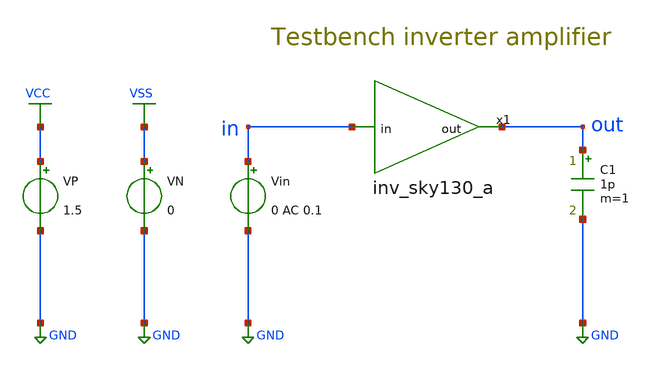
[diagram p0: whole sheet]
** sch_path: Amplifier_Inv/xschem/tb_inv_sky130_a.sch
* StefanSchippers/xschem_sky130/sky130_tests/not.sch:
* Copyright 2021 Stefan Frederik Schippers
* Licensed under the Apache License, Version 2.0 (the "License");
**.subckt tb_inv_sky130_a
x1 out in inv_sky130_a
Vin in GND 0 AC 0.1
VN VSS GND 0
VP VCC GND 1.5
C1 out GND 1p m=1
**** begin user architecture code

** opencircuitdesign pdks install
.lib $::SKYWATER_MODELS/sky130.lib.spice tt




.control
  tran 1ns 100us
  save all
  write tb_inv_sky130_a_tran.raw
  ac dec 10 0.1 100k
  save all
  let gain = db(v(out)/v(in))
  let phase = phase(v(out)/v(in))
  print gain phase
  write tb_inv_sky130_a_AC.raw gain phase
.endc


**** end user architecture code
**.ends

* expanding   symbol:  inv_sky130_a.sym # of pins=2
** sym_path: Amplifier_Inv/xschem/inv_sky130_a.sym
** sch_path: Amplifier_Inv/xschem/inv_sky130_a.sch
.subckt inv_sky130_a out in
*.ipin in
*.opin out
x1 out in VCC VSS not W_N=1 L_N=0.15 W_P=2 L_P=0.15 m=1
R1 out in sky130_fd_pr__res_generic_m1 W=1 L=1 m=1
R2 net1 out sky130_fd_pr__res_generic_m1 W=1 L=1 m=1
XC1 net1 GND sky130_fd_pr__cap_mim_m3_1 W=1 L=1 MF=1 m=1
.ends


* expanding   symbol:  sky130_tests/not.sym # of pins=2
** sym_path: sky130_tests/not.sym
** sch_path: sky130_tests/not.sch
.subckt not y a VCCPIN VSSPIN     W_N=1 L_N=0.15 W_P=2 L_P=0.15
*.opin y
*.ipin a
XM1 DN a VSSPIN VSSPIN sky130_fd_pr__nfet_01v8 L=L_N W=W_N nf=1 ad='int((1 + 1)/2) * W_N / 1 * 0.29'
+ as='int((1 + 2)/2) * W_N / 1 * 0.29' pd='2*int((1 + 1)/2) * (W_N / 1 + 0.29)' ps='2*int((1 + 2)/2) * (W_N / 1 + 0.29)'
+ nrd='0.29 / W_N ' nrs='0.29 / W_N ' sa=0 sb=0 sd=0 mult=1 m=1
XM2 DP a VCCPIN VCCPIN sky130_fd_pr__pfet_01v8 L=L_P W=W_P nf=1 ad='int((nf+1)/2) * W/nf * 0.29' as='int((nf+2)/2) * W/nf * 0.29'
+ pd='2*int((nf+1)/2) * (W/nf + 0.29)' ps='2*int((nf+2)/2) * (W/nf + 0.29)' nrd='0.29 / W' nrs='0.29 / W'
+ sa=0 sb=0 sd=0 mult=1 m=1
Vmeas DP y 0
.save i(vmeas)
Vmeas1 y DN 0
.save i(vmeas1)
.save v(dp)
.save v(dn)
.ends

.GLOBAL GND
.GLOBAL VSS
.GLOBAL VCC
.end
